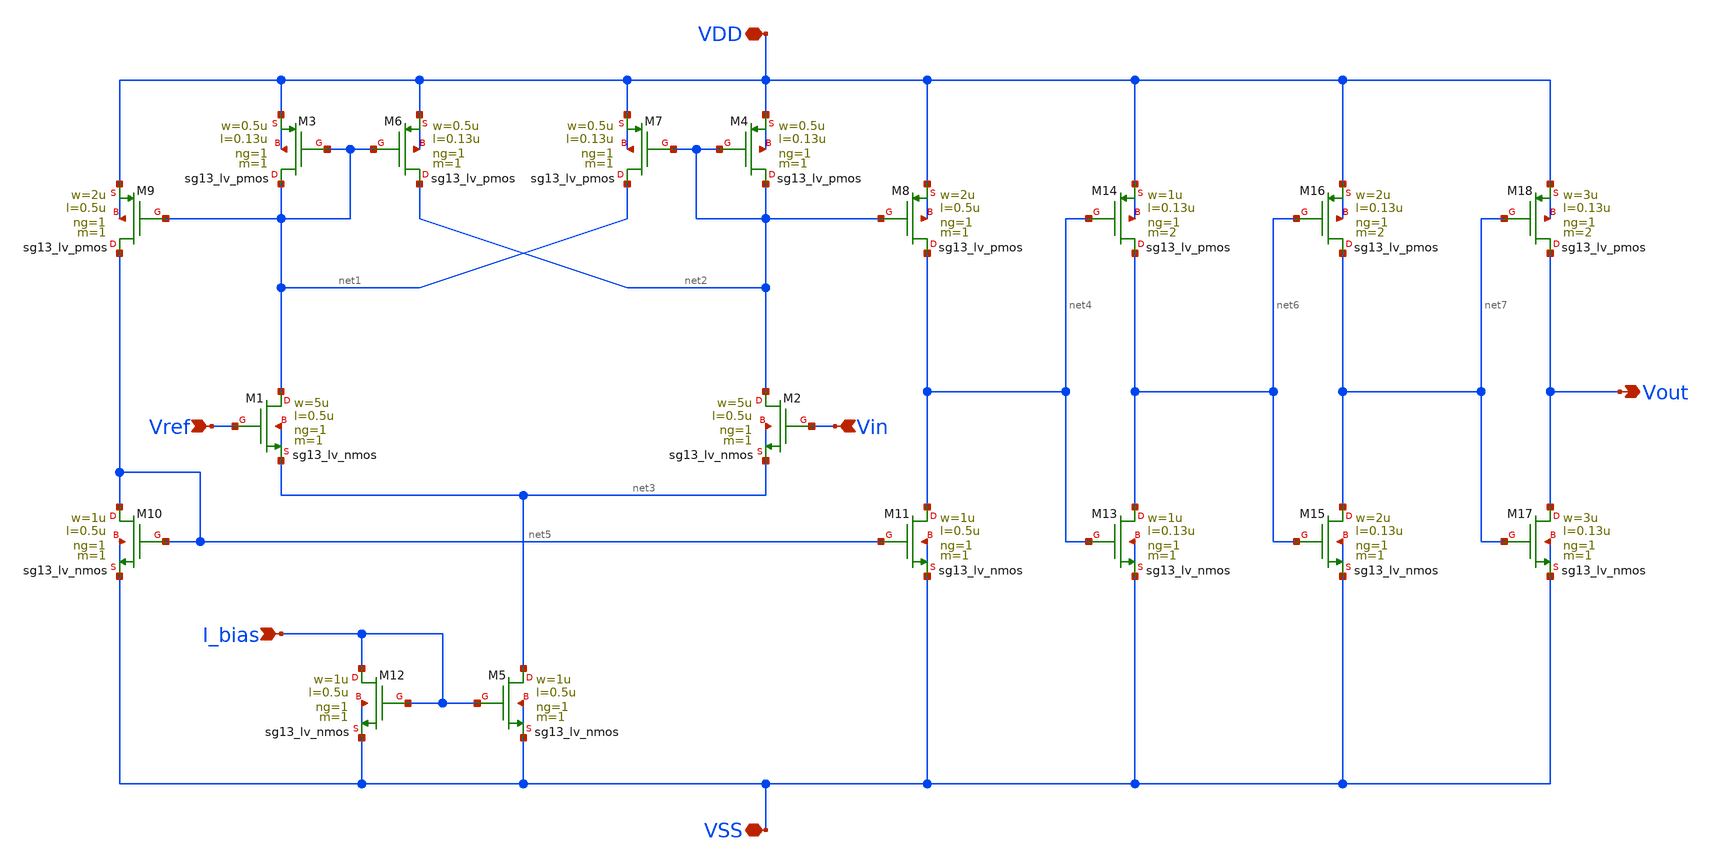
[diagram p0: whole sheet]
** sch_path: SSDOR_1.2V_v4/components/comp_w_hyst/comp_w_hyst.sch
**.subckt comp_w_hyst I_bias Vref Vin VSS VDD Vout
*.ipin I_bias
*.ipin Vref
*.ipin Vin
*.iopin VSS
*.iopin VDD
*.opin Vout
XM3 net1 net1 VDD VDD sg13_lv_pmos w=0.5u l=0.13u ng=1 m=1 mm_ok=1
XM6 net2 net1 VDD VDD sg13_lv_pmos w=0.5u l=0.13u ng=1 m=1 mm_ok=1
XM7 net1 net2 VDD VDD sg13_lv_pmos w=0.5u l=0.13u ng=1 m=1 mm_ok=1
XM4 net2 net2 VDD VDD sg13_lv_pmos w=0.5u l=0.13u ng=1 m=1 mm_ok=1
XM1 net1 Vref net3 net3 sg13_lv_nmos w=5u l=0.5u ng=1 m=1 mm_ok=1
XM2 net2 Vin net3 net3 sg13_lv_nmos w=5u l=0.5u ng=1 m=1 mm_ok=1
XM5 net3 I_bias VSS VSS sg13_lv_nmos w=1u l=0.5u ng=1 m=1 mm_ok=1
XM9 net5 net1 VDD VDD sg13_lv_pmos w=2u l=0.5u ng=1 m=1 mm_ok=1
XM8 net4 net2 VDD VDD sg13_lv_pmos w=2u l=0.5u ng=1 m=1 mm_ok=1
XM11 net4 net5 VSS VSS sg13_lv_nmos w=1u l=0.5u ng=1 m=1 mm_ok=1
XM10 net5 net5 VSS VSS sg13_lv_nmos w=1u l=0.5u ng=1 m=1 mm_ok=1
XM12 I_bias I_bias VSS VSS sg13_lv_nmos w=1u l=0.5u ng=1 m=1 mm_ok=1
XM13 net6 net4 VSS VSS sg13_lv_nmos w=1u l=0.13u ng=1 m=1 mm_ok=1
XM14 net6 net4 VDD VDD sg13_lv_pmos w=1u l=0.13u ng=1 m=2 mm_ok=1
XM15 net7 net6 VSS VSS sg13_lv_nmos w=2u l=0.13u ng=1 m=1 mm_ok=1
XM16 net7 net6 VDD VDD sg13_lv_pmos w=2u l=0.13u ng=1 m=2 mm_ok=1
XM17 Vout net7 VSS VSS sg13_lv_nmos w=3u l=0.13u ng=1 m=1 mm_ok=1
XM18 Vout net7 VDD VDD sg13_lv_pmos w=3u l=0.13u ng=1 m=2 mm_ok=1
**.ends
.end
